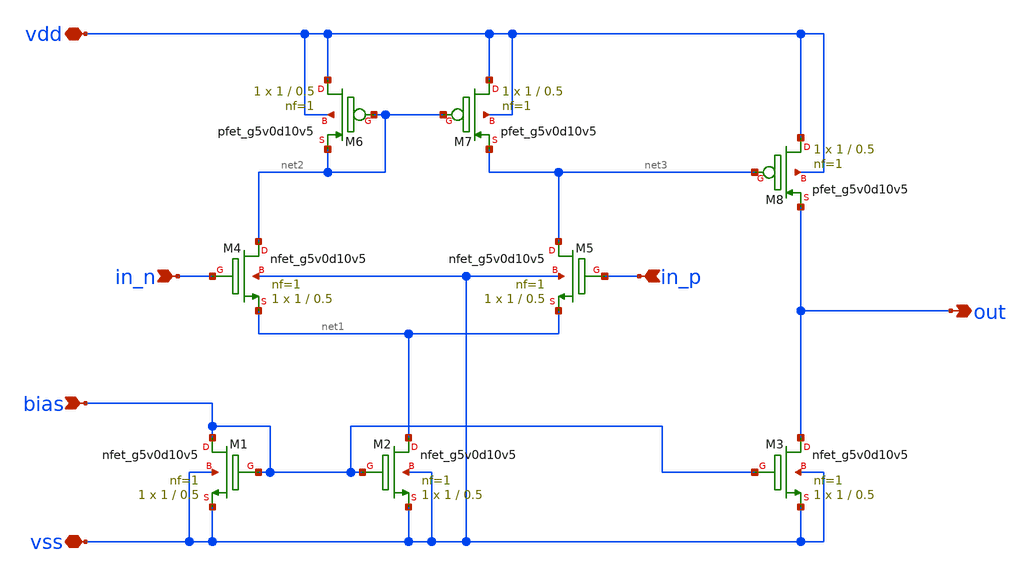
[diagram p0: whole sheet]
** sch_path: design/myopamp/myopamp.sch
**.subckt myopamp in_n in_p bias out vdd vss
*.ipin in_n
*.ipin in_p
*.ipin bias
*.opin out
*.iopin vdd
*.iopin vss
XM7 vdd net2 net3 vdd sky130_fd_pr__pfet_g5v0d10v5 L=0.5 W=1 nf=1 ad='int((nf+1)/2) * W/nf * 0.29' as='int((nf+2)/2) * W/nf * 0.29'
+ pd='2*int((nf+1)/2) * (W/nf + 0.29)' ps='2*int((nf+2)/2) * (W/nf + 0.29)' nrd='0.29 / W' nrs='0.29 / W'
+ sa=0 sb=0 sd=0 mult=1 m=1
XM6 vdd net2 net2 vdd sky130_fd_pr__pfet_g5v0d10v5 L=0.5 W=1 nf=1 ad='int((nf+1)/2) * W/nf * 0.29' as='int((nf+2)/2) * W/nf * 0.29'
+ pd='2*int((nf+1)/2) * (W/nf + 0.29)' ps='2*int((nf+2)/2) * (W/nf + 0.29)' nrd='0.29 / W' nrs='0.29 / W'
+ sa=0 sb=0 sd=0 mult=1 m=1
XM8 vdd net3 out vdd sky130_fd_pr__pfet_g5v0d10v5 L=0.5 W=1 nf=1 ad='int((nf+1)/2) * W/nf * 0.29' as='int((nf+2)/2) * W/nf * 0.29'
+ pd='2*int((nf+1)/2) * (W/nf + 0.29)' ps='2*int((nf+2)/2) * (W/nf + 0.29)' nrd='0.29 / W' nrs='0.29 / W'
+ sa=0 sb=0 sd=0 mult=1 m=1
XM4 net2 in_n net1 vss sky130_fd_pr__nfet_g5v0d10v5 L=0.5 W=1 nf=1 ad='int((nf+1)/2) * W/nf * 0.29' as='int((nf+2)/2) * W/nf * 0.29'
+ pd='2*int((nf+1)/2) * (W/nf + 0.29)' ps='2*int((nf+2)/2) * (W/nf + 0.29)' nrd='0.29 / W' nrs='0.29 / W'
+ sa=0 sb=0 sd=0 mult=1 m=1
XM5 net3 in_p net1 vss sky130_fd_pr__nfet_g5v0d10v5 L=0.5 W=1 nf=1 ad='int((nf+1)/2) * W/nf * 0.29' as='int((nf+2)/2) * W/nf * 0.29'
+ pd='2*int((nf+1)/2) * (W/nf + 0.29)' ps='2*int((nf+2)/2) * (W/nf + 0.29)' nrd='0.29 / W' nrs='0.29 / W'
+ sa=0 sb=0 sd=0 mult=1 m=1
XM1 bias bias vss vss sky130_fd_pr__nfet_g5v0d10v5 L=0.5 W=1 nf=1 ad='int((nf+1)/2) * W/nf * 0.29' as='int((nf+2)/2) * W/nf * 0.29'
+ pd='2*int((nf+1)/2) * (W/nf + 0.29)' ps='2*int((nf+2)/2) * (W/nf + 0.29)' nrd='0.29 / W' nrs='0.29 / W'
+ sa=0 sb=0 sd=0 mult=1 m=1
XM2 net1 bias vss vss sky130_fd_pr__nfet_g5v0d10v5 L=0.5 W=1 nf=1 ad='int((nf+1)/2) * W/nf * 0.29' as='int((nf+2)/2) * W/nf * 0.29'
+ pd='2*int((nf+1)/2) * (W/nf + 0.29)' ps='2*int((nf+2)/2) * (W/nf + 0.29)' nrd='0.29 / W' nrs='0.29 / W'
+ sa=0 sb=0 sd=0 mult=1 m=1
XM3 out bias vss vss sky130_fd_pr__nfet_g5v0d10v5 L=0.5 W=1 nf=1 ad='int((nf+1)/2) * W/nf * 0.29' as='int((nf+2)/2) * W/nf * 0.29'
+ pd='2*int((nf+1)/2) * (W/nf + 0.29)' ps='2*int((nf+2)/2) * (W/nf + 0.29)' nrd='0.29 / W' nrs='0.29 / W'
+ sa=0 sb=0 sd=0 mult=1 m=1
**.ends
.end
